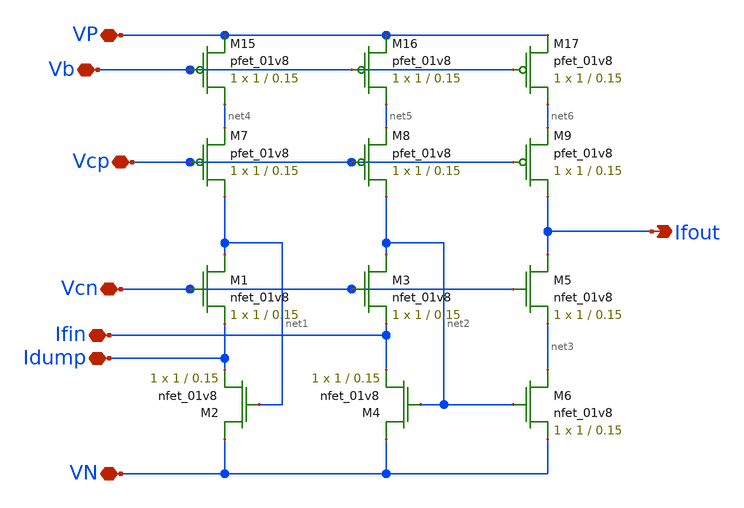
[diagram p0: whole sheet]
** sch_path: FVF-1.sch
**.subckt FVF-1 VN Vcn Ifin Idump Vcp VP Vb Ifout
*.iopin VN
*.iopin Vcn
*.iopin Ifin
*.iopin Idump
*.iopin Vcp
*.iopin VP
*.iopin Vb
*.opin Ifout
XM1 net1 Vcn Idump GND sky130_fd_pr__nfet_01v8 L=0.15 W=1 nf=1 ad='int((nf+1)/2) * W/nf * 0.29' as='int((nf+2)/2) * W/nf * 0.29'
+ pd='2*int((nf+1)/2) * (W/nf + 0.29)' ps='2*int((nf+2)/2) * (W/nf + 0.29)' nrd='0.29 / W' nrs='0.29 / W'
+ sa=0 sb=0 sd=0 mult=1 m=1
XM2 VN net1 Idump GND sky130_fd_pr__nfet_01v8 L=0.15 W=1 nf=1 ad='int((nf+1)/2) * W/nf * 0.29' as='int((nf+2)/2) * W/nf * 0.29'
+ pd='2*int((nf+1)/2) * (W/nf + 0.29)' ps='2*int((nf+2)/2) * (W/nf + 0.29)' nrd='0.29 / W' nrs='0.29 / W'
+ sa=0 sb=0 sd=0 mult=1 m=1
XM3 net2 Vcn Ifin GND sky130_fd_pr__nfet_01v8 L=0.15 W=1 nf=1 ad='int((nf+1)/2) * W/nf * 0.29' as='int((nf+2)/2) * W/nf * 0.29'
+ pd='2*int((nf+1)/2) * (W/nf + 0.29)' ps='2*int((nf+2)/2) * (W/nf + 0.29)' nrd='0.29 / W' nrs='0.29 / W'
+ sa=0 sb=0 sd=0 mult=1 m=1
XM4 VN net2 Ifin GND sky130_fd_pr__nfet_01v8 L=0.15 W=1 nf=1 ad='int((nf+1)/2) * W/nf * 0.29' as='int((nf+2)/2) * W/nf * 0.29'
+ pd='2*int((nf+1)/2) * (W/nf + 0.29)' ps='2*int((nf+2)/2) * (W/nf + 0.29)' nrd='0.29 / W' nrs='0.29 / W'
+ sa=0 sb=0 sd=0 mult=1 m=1
XM5 Ifout Vcn net3 GND sky130_fd_pr__nfet_01v8 L=0.15 W=1 nf=1 ad='int((nf+1)/2) * W/nf * 0.29' as='int((nf+2)/2) * W/nf * 0.29'
+ pd='2*int((nf+1)/2) * (W/nf + 0.29)' ps='2*int((nf+2)/2) * (W/nf + 0.29)' nrd='0.29 / W' nrs='0.29 / W'
+ sa=0 sb=0 sd=0 mult=1 m=1
XM6 net3 net2 VN GND sky130_fd_pr__nfet_01v8 L=0.15 W=1 nf=1 ad='int((nf+1)/2) * W/nf * 0.29' as='int((nf+2)/2) * W/nf * 0.29'
+ pd='2*int((nf+1)/2) * (W/nf + 0.29)' ps='2*int((nf+2)/2) * (W/nf + 0.29)' nrd='0.29 / W' nrs='0.29 / W'
+ sa=0 sb=0 sd=0 mult=1 m=1
XM7 net1 Vcp net4 VDD sky130_fd_pr__pfet_01v8 L=0.15 W=1 nf=1 ad='int((nf+1)/2) * W/nf * 0.29' as='int((nf+2)/2) * W/nf * 0.29'
+ pd='2*int((nf+1)/2) * (W/nf + 0.29)' ps='2*int((nf+2)/2) * (W/nf + 0.29)' nrd='0.29 / W' nrs='0.29 / W'
+ sa=0 sb=0 sd=0 mult=1 m=1
XM8 net2 Vcp net5 VDD sky130_fd_pr__pfet_01v8 L=0.15 W=1 nf=1 ad='int((nf+1)/2) * W/nf * 0.29' as='int((nf+2)/2) * W/nf * 0.29'
+ pd='2*int((nf+1)/2) * (W/nf + 0.29)' ps='2*int((nf+2)/2) * (W/nf + 0.29)' nrd='0.29 / W' nrs='0.29 / W'
+ sa=0 sb=0 sd=0 mult=1 m=1
XM9 Ifout Vcp net6 VDD sky130_fd_pr__pfet_01v8 L=0.15 W=1 nf=1 ad='int((nf+1)/2) * W/nf * 0.29' as='int((nf+2)/2) * W/nf * 0.29'
+ pd='2*int((nf+1)/2) * (W/nf + 0.29)' ps='2*int((nf+2)/2) * (W/nf + 0.29)' nrd='0.29 / W' nrs='0.29 / W'
+ sa=0 sb=0 sd=0 mult=1 m=1
XM15 net4 Vb VP VDD sky130_fd_pr__pfet_01v8 L=0.15 W=1 nf=1 ad='int((nf+1)/2) * W/nf * 0.29' as='int((nf+2)/2) * W/nf * 0.29'
+ pd='2*int((nf+1)/2) * (W/nf + 0.29)' ps='2*int((nf+2)/2) * (W/nf + 0.29)' nrd='0.29 / W' nrs='0.29 / W'
+ sa=0 sb=0 sd=0 mult=1 m=1
XM16 net5 Vb VP VDD sky130_fd_pr__pfet_01v8 L=0.15 W=1 nf=1 ad='int((nf+1)/2) * W/nf * 0.29' as='int((nf+2)/2) * W/nf * 0.29'
+ pd='2*int((nf+1)/2) * (W/nf + 0.29)' ps='2*int((nf+2)/2) * (W/nf + 0.29)' nrd='0.29 / W' nrs='0.29 / W'
+ sa=0 sb=0 sd=0 mult=1 m=1
XM17 net6 Vb VP VDD sky130_fd_pr__pfet_01v8 L=0.15 W=1 nf=1 ad='int((nf+1)/2) * W/nf * 0.29' as='int((nf+2)/2) * W/nf * 0.29'
+ pd='2*int((nf+1)/2) * (W/nf + 0.29)' ps='2*int((nf+2)/2) * (W/nf + 0.29)' nrd='0.29 / W' nrs='0.29 / W'
+ sa=0 sb=0 sd=0 mult=1 m=1
**.ends
.end
